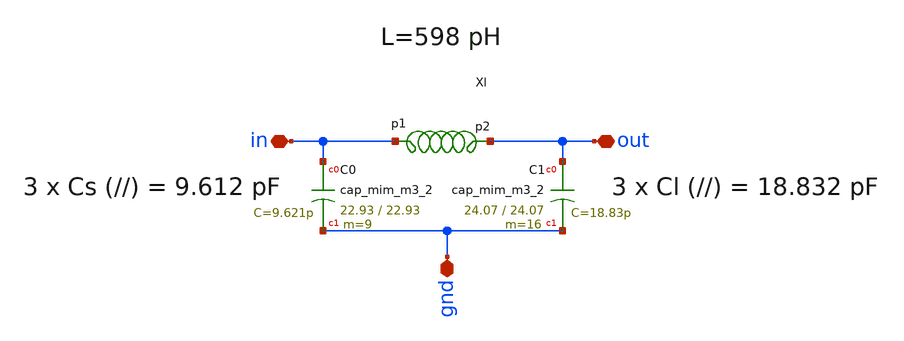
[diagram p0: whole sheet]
** sch_path: impedance-transformer/xschem/impedance-transformer.sch
**.subckt impedance-transformer gnd in out
*.iopin gnd
*.iopin in
*.iopin out
XC0 in gnd sky130_fd_pr__cap_mim_m3_2 W=22.93 L=22.93 MF=9 m=9
XC1 out gnd sky130_fd_pr__cap_mim_m3_2 W=24.07 L=24.07 MF=16 m=16
x1 in out l1
**.ends

* expanding   symbol:  /home/hugodg/projects_sky130/temp_sensor/impedance-transformer/xschem/l1.sym
*+ # of pins=2
** sym_path: impedance-transformer/xschem/l1.sym
** sch_path: impedance-transformer/xschem/l1.sch
.subckt l1 p1 p2
*.iopin p2
*.iopin p1
L0 p1 net3 598p m=1
Cs1 p1 net1 26.59f m=1
Cs2 p2 net2 25.14f m=1
Rs1 net1 GND 63.55 m=1
Rs2 net2 GND 19.11 m=1
R1 p2 net3 2.89 m=1
.ends

.GLOBAL GND
.end
